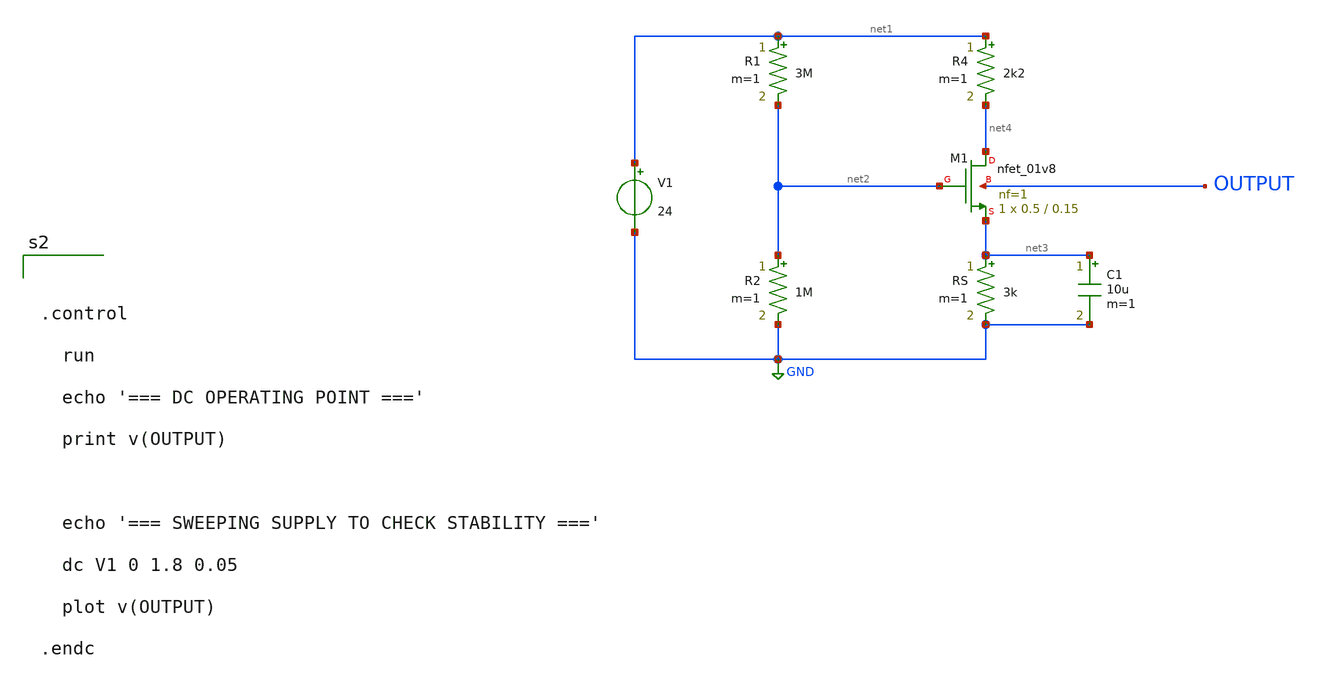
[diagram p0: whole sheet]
** sch_path: cmosvoltagedivider.sch
**.subckt cmosvoltagedivider
XM1 net4 net2 net3 OUTPUT sky130_fd_pr__nfet_01v8 L=0.15 W=0.5 nf=1 ad='int((1 + 1)/2) * 0.5 / 1 * 0.29'
+ as='int((1 + 2)/2) * 0.5 / 1 * 0.29' pd='2*int((1 + 1)/2) * (0.5 / 1 + 0.29)' ps='2*int((1 + 2)/2) * (0.5 / 1 + 0.29)'
+ nrd='0.29 / 0.5 ' nrs='0.29 / 0.5 ' sa=0 sb=0 sd=0 mult=1 m=1
R1 net1 net2 3M m=1
R2 net2 GND 1M m=1
RS net3 GND 3k m=1
R4 net1 net4 2k2 m=1
V1 net1 GND 24
C1 net3 GND 10u m=1
**** begin user architecture code



.lib /foss/pdks/sky130A/libs.tech/ngspice/sky130.lib.spice tt

* Discrete JFET Model for the Voltage Divider Circuit
.model jfet_n njf(beta=1m vto=-2.0)
.op





.control

  run

  echo '=== DC OPERATING POINT ==='

  print v(OUTPUT)



  echo '=== SWEEPING SUPPLY TO CHECK STABILITY ==='

  dc V1 0 1.8 0.05

  plot v(OUTPUT)

.endc



**** end user architecture code
**.ends
.GLOBAL GND
.end
